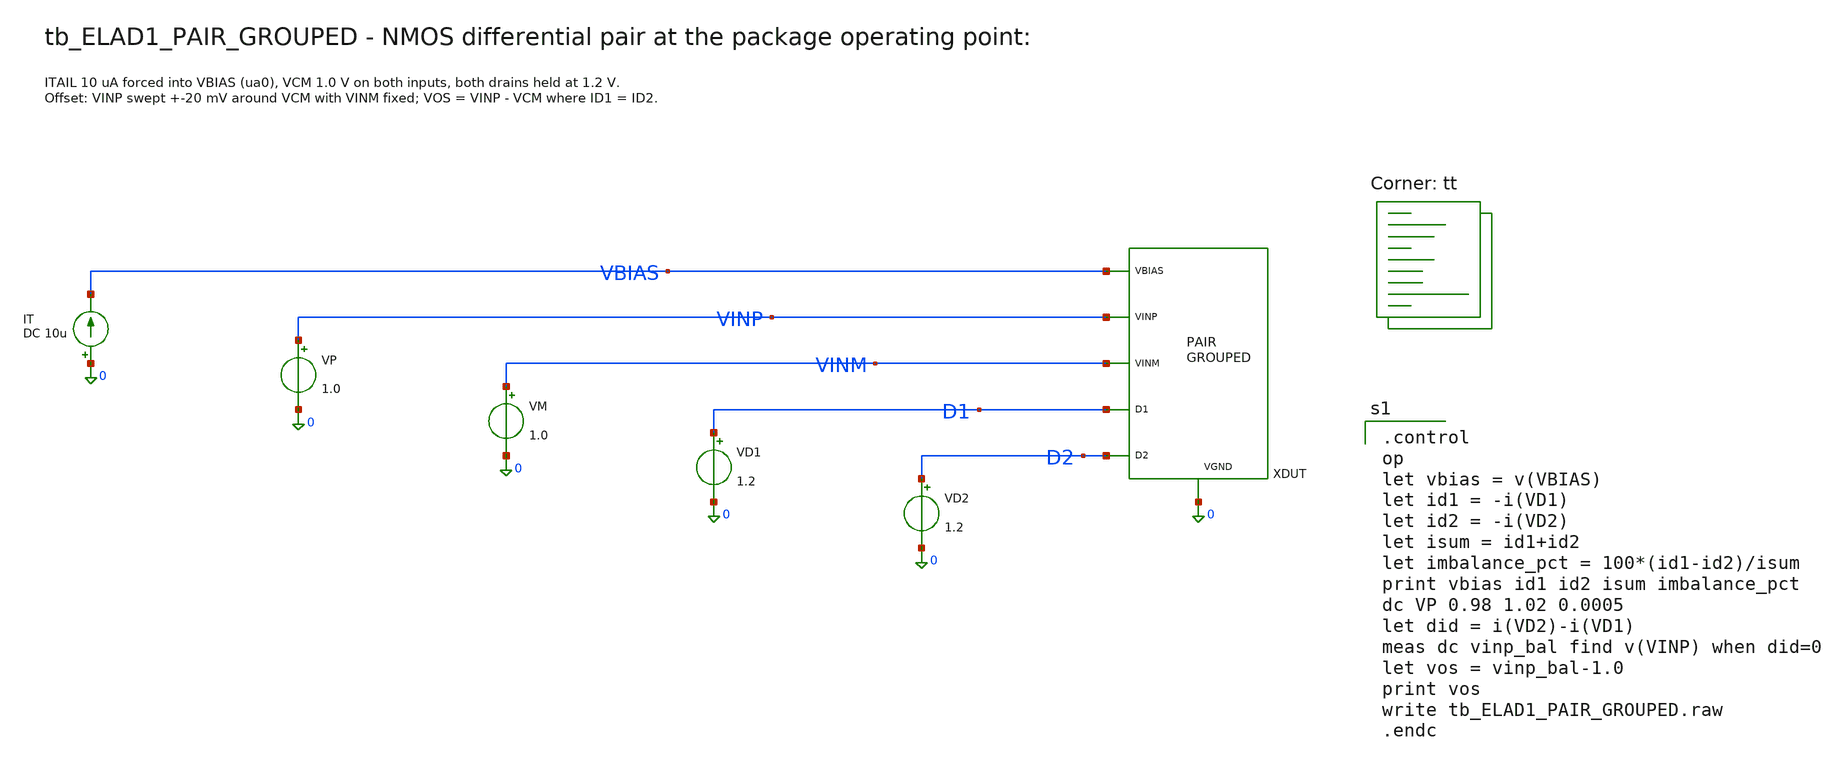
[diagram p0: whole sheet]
** sch_path: cells/ELAD1_PAIR_GROUPED/schematic/tb_ELAD1_PAIR_GROUPED.sch
**.subckt tb_ELAD1_PAIR_GROUPED
XDUT VINP VINM D1 D2 VBIAS 0 ELAD1_PAIR_GROUPED
VD2 D2 0 1.2
VD1 D1 0 1.2
VM VINM 0 1.0
VP VINP 0 1.0
IT 0 VBIAS DC 10u
**** begin user architecture code

.control
op
let vbias = v(VBIAS)
let id1 = -i(VD1)
let id2 = -i(VD2)
let isum = id1+id2
let imbalance_pct = 100*(id1-id2)/isum
print vbias id1 id2 isum imbalance_pct
dc VP 0.98 1.02 0.0005
let did = i(VD2)-i(VD1)
meas dc vinp_bal find v(VINP) when did=0
let vos = vinp_bal-1.0
print vos
write tb_ELAD1_PAIR_GROUPED.raw
.endc

.lib $::SKYWATER_MODELS/sky130.lib.spice tt
**** end user architecture code
**.ends
.end
